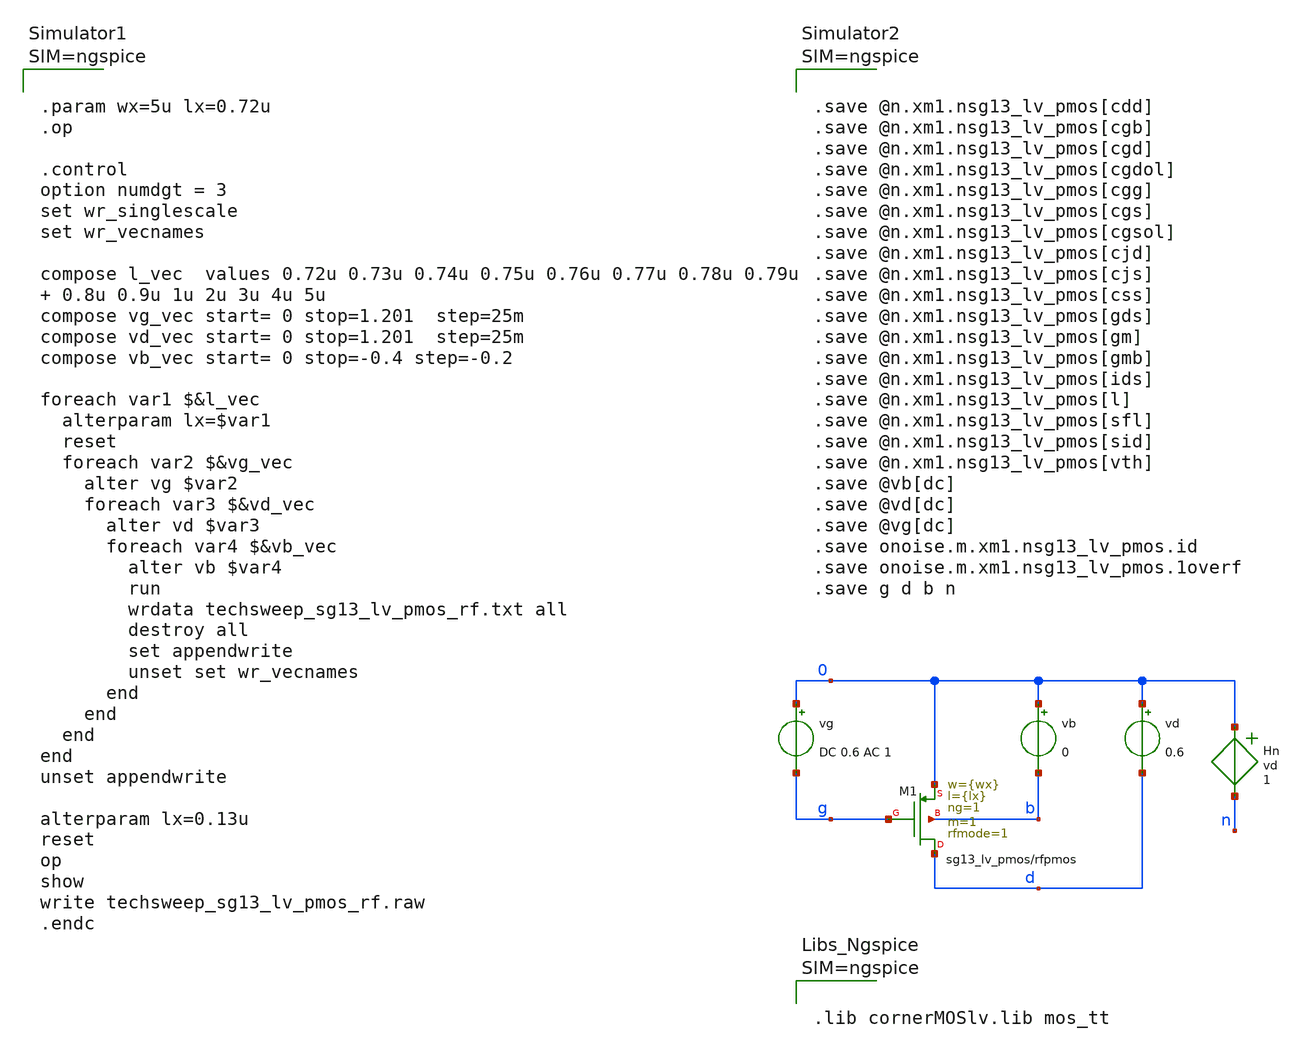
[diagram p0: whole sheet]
** sch_path: starter_files_open_source_tools/ihp-sg13cmos5l/techsweep_sg13_lv_pmos_rf.sch
**.subckt techsweep_sg13_lv_pmos_rf
Hn 0 n vd 1
vg 0 g DC 0.6 AC 1
vd 0 d 0.6
vb 0 b 0
XM1 d g 0 b sg13_lv_pmos w={wx} l={lx} ng=1 m=1 rfmode=1 mm_ok=1
**** begin user architecture code



.save @n.xm1.nsg13_lv_pmos[cdd]
.save @n.xm1.nsg13_lv_pmos[cgb]
.save @n.xm1.nsg13_lv_pmos[cgd]
.save @n.xm1.nsg13_lv_pmos[cgdol]
.save @n.xm1.nsg13_lv_pmos[cgg]
.save @n.xm1.nsg13_lv_pmos[cgs]
.save @n.xm1.nsg13_lv_pmos[cgsol]
.save @n.xm1.nsg13_lv_pmos[cjd]
.save @n.xm1.nsg13_lv_pmos[cjs]
.save @n.xm1.nsg13_lv_pmos[css]
.save @n.xm1.nsg13_lv_pmos[gds]
.save @n.xm1.nsg13_lv_pmos[gm]
.save @n.xm1.nsg13_lv_pmos[gmb]
.save @n.xm1.nsg13_lv_pmos[ids]
.save @n.xm1.nsg13_lv_pmos[l]
.save @n.xm1.nsg13_lv_pmos[sfl]
.save @n.xm1.nsg13_lv_pmos[sid]
.save @n.xm1.nsg13_lv_pmos[vth]
.save @vb[dc]
.save @vd[dc]
.save @vg[dc]
.save onoise.m.xm1.nsg13_lv_pmos.id
.save onoise.m.xm1.nsg13_lv_pmos.1overf
.save g d b n






.param wx=5u lx=0.72u
.op

.control
option numdgt = 3
set wr_singlescale
set wr_vecnames

compose l_vec  values 0.72u 0.73u 0.74u 0.75u 0.76u 0.77u 0.78u 0.79u  0.8u 0.9u 1u 2u 3u 4u 5u
compose vg_vec start= 0 stop=1.201  step=25m
compose vd_vec start= 0 stop=1.201  step=25m
compose vb_vec start= 0 stop=-0.4 step=-0.2

foreach var1 $&l_vec
  alterparam lx=$var1
  reset
  foreach var2 $&vg_vec
    alter vg $var2
    foreach var3 $&vd_vec
      alter vd $var3
      foreach var4 $&vb_vec
        alter vb $var4
        run
        wrdata techsweep_sg13_lv_pmos_rf.txt all
        destroy all
        set appendwrite
        unset set wr_vecnames
      end
    end
  end
end
unset appendwrite

alterparam lx=0.13u
reset
op
show
write techsweep_sg13_lv_pmos_rf.raw
.endc






.lib cornerMOSlv.lib mos_tt



**** end user architecture code
**.ends
.end
